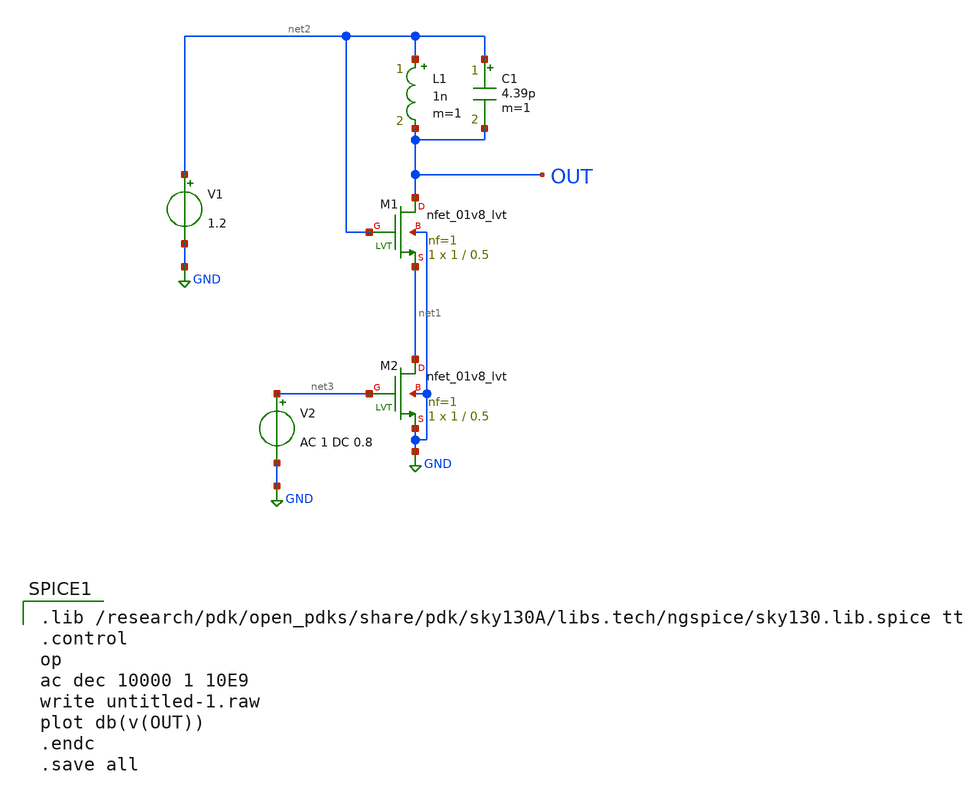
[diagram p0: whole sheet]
** sch_path: skywater_stuff/ECE631_RF_CMOS/untitled-1.sch
**.subckt untitled-1
XM1 OUT net2 net1 GND sky130_fd_pr__nfet_01v8_lvt L=0.5 W=1 nf=1 ad='int((nf+1)/2) * W/nf * 0.29' as='int((nf+2)/2) * W/nf * 0.29'
+ pd='2*int((nf+1)/2) * (W/nf + 0.29)' ps='2*int((nf+2)/2) * (W/nf + 0.29)' nrd='0.29 / W' nrs='0.29 / W'
+ sa=0 sb=0 sd=0 mult=1 m=1
XM2 net1 net3 GND GND sky130_fd_pr__nfet_01v8_lvt L=0.5 W=1 nf=1 ad='int((nf+1)/2) * W/nf * 0.29' as='int((nf+2)/2) * W/nf * 0.29'
+ pd='2*int((nf+1)/2) * (W/nf + 0.29)' ps='2*int((nf+2)/2) * (W/nf + 0.29)' nrd='0.29 / W' nrs='0.29 / W'
+ sa=0 sb=0 sd=0 mult=1 m=1
V1 net2 GND 1.2
C1 net2 OUT 4.39p m=1
L1 net2 OUT 1n m=1
V2 net3 GND AC 1 DC 0.8
**** begin user architecture code

.lib /research/pdk/open_pdks/share/pdk/sky130A/libs.tech/ngspice/sky130.lib.spice tt
.control
op
ac dec 10000 1 10E9
write untitled-1.raw
plot db(v(OUT))
.endc
.save all


**** end user architecture code
**.ends
.GLOBAL GND
.end
